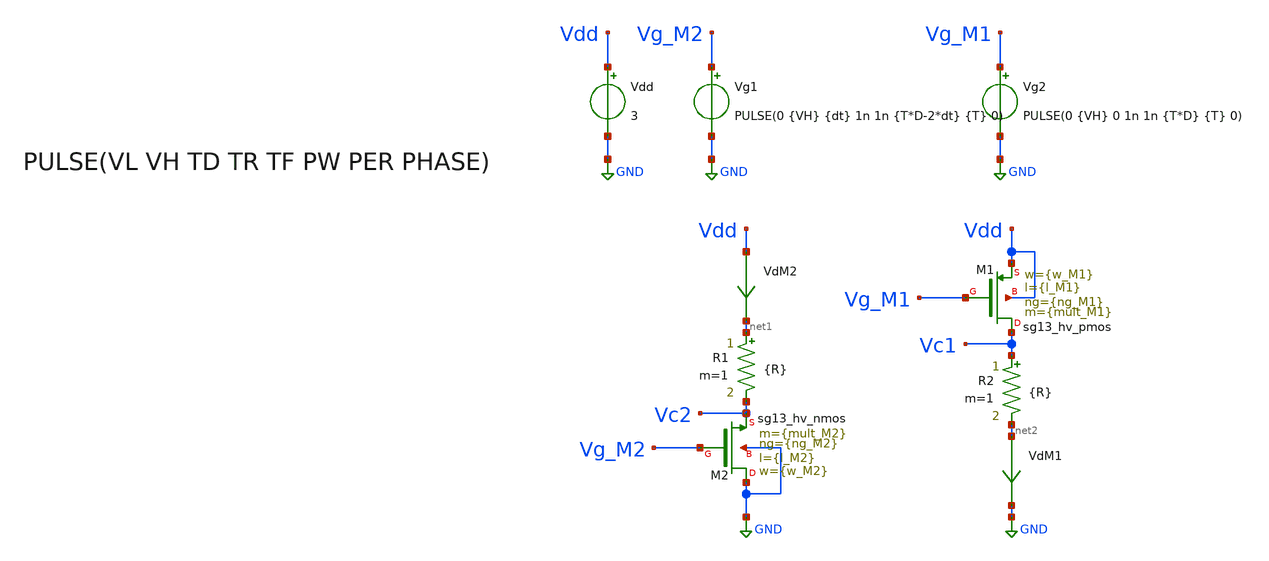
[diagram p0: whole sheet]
** sch_path: xschem/TB_hvMOS_switch_test.sch
**.subckt TB_hvMOS_switch_test
XM2 GND Vg_M2 Vc2 GND sg13_hv_nmos w={w_M2} l={l_M2} ng={ng_M2} m={mult_M2} mm_ok=1
XM1 Vc1 Vg_M1 Vdd Vdd sg13_hv_pmos w={w_M1} l={l_M1} ng={ng_M1} m={mult_M1} mm_ok=1
Vdd Vdd GND 3
VdM2 Vdd net1 0
.save i(vdm2)
VdM1 net2 GND 0
.save i(vdm1)
Vg1 Vg_M2 GND PULSE(0 {VH} {dt} 1n 1n {T*D-2*dt} {T} 0)
Vg2 Vg_M1 GND PULSE(0 {VH} 0 1n 1n {T*D} {T} 0)
R1 net1 Vc2 {R} m=1
R2 Vc1 net2 {R} m=1
**** begin user architecture code

.lib cornerMOShv.lib mos_tt



.param R = 1.4
.param VH = 3
.param D = 0.5
.param T = 1u
.param dt = 0.1u
.param temp = 27






.save all
.control
reset
set color0 = white
tran 1n 4u
plot i(VdM1) i(VdM2)
plot v(Vc1) v(Vc2)
plot v(Vg_M1) v(Vg_M2)
.endc

.end




.param temp=27
.param mult_M1 = 2400
.param w_M1 =10u
*.param l_M1 = 0.2u ** Posee mayor capacidad de corriente, pero en sub-umbral conduce mucha
*+ corriente
.param l_M1 = 0.22u
.param ng_M1 = 1

.param mult_M2 = 1200
.param w_M2 =10u
*.param l_M2 =0.25u
.param l_M2 =0.25u
.param ng_M2 =1





**** end user architecture code
**.ends
.GLOBAL GND
.end
